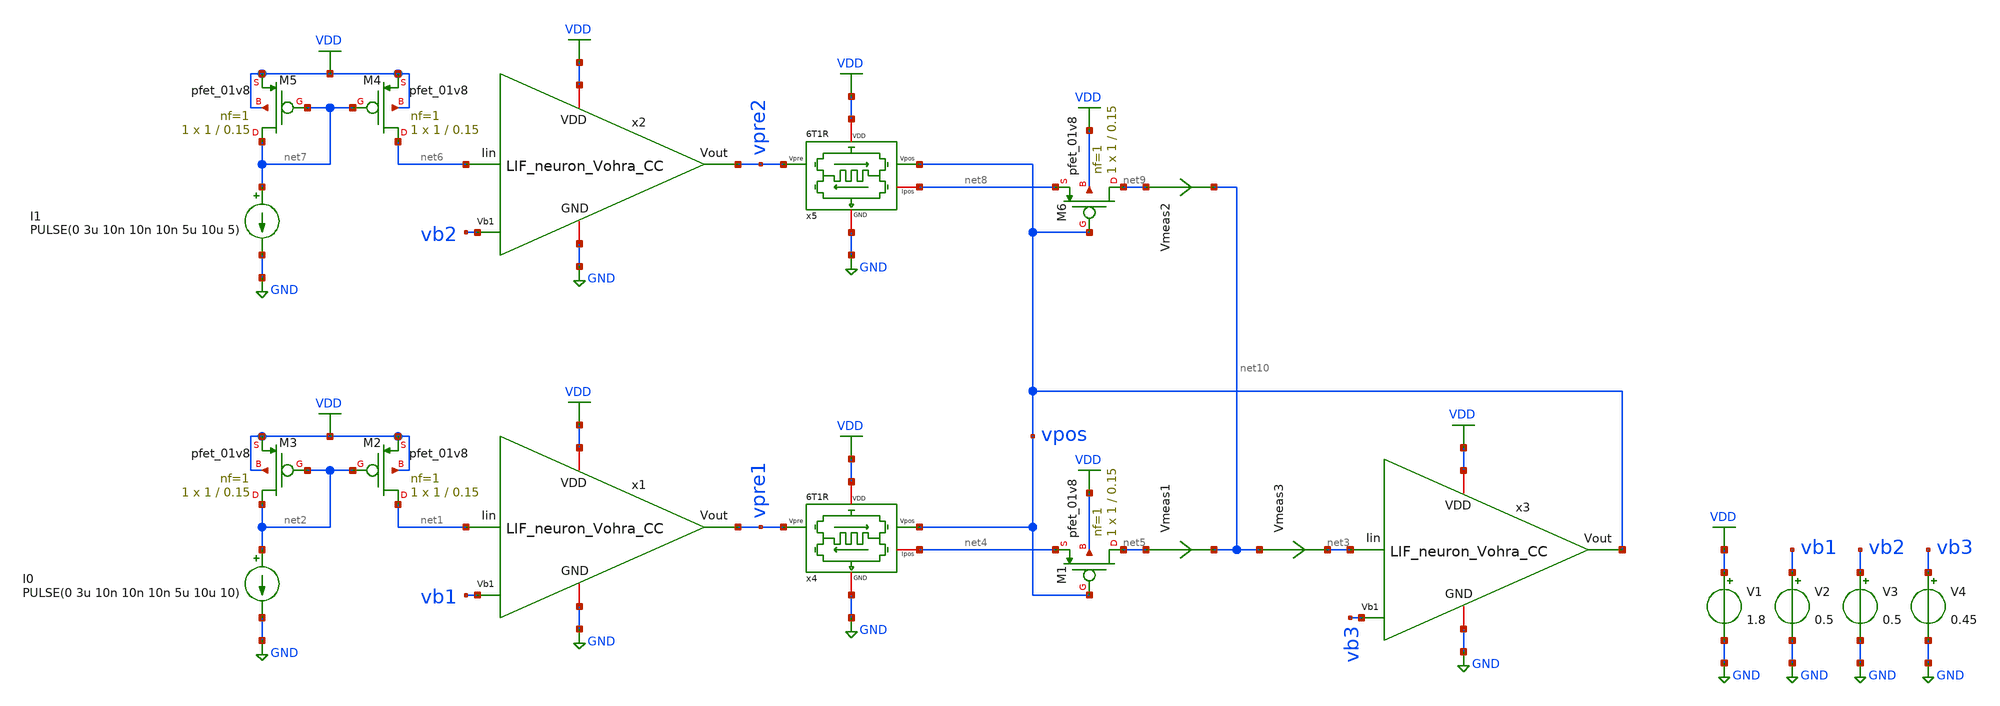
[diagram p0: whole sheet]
** sch_path: STDP/STDP_3_LIF_6T1R.sch
**.subckt STDP_3_LIF_6T1R
V1 VDD GND 1.8
V2 vb1 GND 0.5
x4 VDD net4 vpre1 vpos GND 6T1R
x1 VDD vpre1 vb1 GND net1 LIF_neuron_Vohra_CC
I0 net2 GND PULSE(0 3u 10n 10n 10n 5u 10u 10)
XM2 net1 net2 VDD VDD sky130_fd_pr__pfet_01v8 L=0.15 W=1 nf=1 ad='int((nf+1)/2) * W/nf * 0.29' as='int((nf+2)/2) * W/nf * 0.29'
+ pd='2*int((nf+1)/2) * (W/nf + 0.29)' ps='2*int((nf+2)/2) * (W/nf + 0.29)' nrd='0.29 / W' nrs='0.29 / W'
+ sa=0 sb=0 sd=0 mult=1 m=1
XM3 net2 net2 VDD VDD sky130_fd_pr__pfet_01v8 L=0.15 W=1 nf=1 ad='int((nf+1)/2) * W/nf * 0.29' as='int((nf+2)/2) * W/nf * 0.29'
+ pd='2*int((nf+1)/2) * (W/nf + 0.29)' ps='2*int((nf+2)/2) * (W/nf + 0.29)' nrd='0.29 / W' nrs='0.29 / W'
+ sa=0 sb=0 sd=0 mult=1 m=1
x3 VDD vpos vb3 GND net3 LIF_neuron_Vohra_CC
XM1 net5 vpos net4 VDD sky130_fd_pr__pfet_01v8 L=0.15 W=1 nf=1 ad='int((nf+1)/2) * W/nf * 0.29' as='int((nf+2)/2) * W/nf * 0.29'
+ pd='2*int((nf+1)/2) * (W/nf + 0.29)' ps='2*int((nf+2)/2) * (W/nf + 0.29)' nrd='0.29 / W' nrs='0.29 / W'
+ sa=0 sb=0 sd=0 mult=1 m=1
Vmeas1 net5 net10 0
.save i(vmeas1)
V3 vb2 GND 0.5
x5 VDD net8 vpre2 vpos GND 6T1R
x2 VDD vpre2 vb2 GND net6 LIF_neuron_Vohra_CC
I1 net7 GND PULSE(0 3u 10n 10n 10n 5u 10u 5)
XM4 net6 net7 VDD VDD sky130_fd_pr__pfet_01v8 L=0.15 W=1 nf=1 ad='int((nf+1)/2) * W/nf * 0.29' as='int((nf+2)/2) * W/nf * 0.29'
+ pd='2*int((nf+1)/2) * (W/nf + 0.29)' ps='2*int((nf+2)/2) * (W/nf + 0.29)' nrd='0.29 / W' nrs='0.29 / W'
+ sa=0 sb=0 sd=0 mult=1 m=1
XM5 net7 net7 VDD VDD sky130_fd_pr__pfet_01v8 L=0.15 W=1 nf=1 ad='int((nf+1)/2) * W/nf * 0.29' as='int((nf+2)/2) * W/nf * 0.29'
+ pd='2*int((nf+1)/2) * (W/nf + 0.29)' ps='2*int((nf+2)/2) * (W/nf + 0.29)' nrd='0.29 / W' nrs='0.29 / W'
+ sa=0 sb=0 sd=0 mult=1 m=1
XM6 net9 vpos net8 VDD sky130_fd_pr__pfet_01v8 L=0.15 W=1 nf=1 ad='int((nf+1)/2) * W/nf * 0.29' as='int((nf+2)/2) * W/nf * 0.29'
+ pd='2*int((nf+1)/2) * (W/nf + 0.29)' ps='2*int((nf+2)/2) * (W/nf + 0.29)' nrd='0.29 / W' nrs='0.29 / W'
+ sa=0 sb=0 sd=0 mult=1 m=1
Vmeas2 net9 net10 0
.save i(vmeas2)
V4 vb3 GND 0.45
Vmeas3 net10 net3 0
.save i(vmeas3)
**** begin user architecture code
.lib $::SKYWATER_MODELS/sky130.lib.spice tt

** opencircuitdesign pdks install
.inc $::SKYWATER_MODELS/rram_v0.spice



.control
  save all
  tran 20n 100u
  write STDP_3_LIF_6T1R.raw
.endc


**** end user architecture code
**.ends

* expanding   symbol:  /home/ricardo/RATT_repos/Proyectos_xschem/synapse/6T1R.sym # of pins=5
** sym_path: synapse/6T1R.sym
** sch_path: synapse/6T1R.sch
.subckt 6T1R VDD Ipos Vpre Vpos GND
*.ipin Vpre
*.ipin Vpos
*.iopin GND
*.iopin Ipos
*.iopin VDD
XM1 vipre Vpre net1 GND sky130_fd_pr__nfet_01v8 L=0.15 W=10 nf=1 ad='int((nf+1)/2) * W/nf * 0.29' as='int((nf+2)/2) * W/nf * 0.29'
+ pd='2*int((nf+1)/2) * (W/nf + 0.29)' ps='2*int((nf+2)/2) * (W/nf + 0.29)' nrd='0.29 / W' nrs='0.29 / W'
+ sa=0 sb=0 sd=0 mult=1 m=1
XR1 net2 net1 rram_v0
XM3 vipre Vpos net2 GND sky130_fd_pr__nfet_01v8 L=0.15 W=1 nf=1 ad='int((nf+1)/2) * W/nf * 0.29' as='int((nf+2)/2) * W/nf * 0.29'
+ pd='2*int((nf+1)/2) * (W/nf + 0.29)' ps='2*int((nf+2)/2) * (W/nf + 0.29)' nrd='0.29 / W' nrs='0.29 / W'
+ sa=0 sb=0 sd=0 mult=1 m=1
XM6 Ipos vipre VDD VDD sky130_fd_pr__pfet_01v8 L=0.15 W=1 nf=1 ad='int((nf+1)/2) * W/nf * 0.29' as='int((nf+2)/2) * W/nf * 0.29'
+ pd='2*int((nf+1)/2) * (W/nf + 0.29)' ps='2*int((nf+2)/2) * (W/nf + 0.29)' nrd='0.29 / W' nrs='0.29 / W'
+ sa=0 sb=0 sd=0 mult=1 m=1
XM5 vipre vipre VDD VDD sky130_fd_pr__pfet_01v8 L=0.15 W=20 nf=1 ad='int((nf+1)/2) * W/nf * 0.29' as='int((nf+2)/2) * W/nf * 0.29'
+ pd='2*int((nf+1)/2) * (W/nf + 0.29)' ps='2*int((nf+2)/2) * (W/nf + 0.29)' nrd='0.29 / W' nrs='0.29 / W'
+ sa=0 sb=0 sd=0 mult=1 m=1
XM2 net1 Vpos GND GND sky130_fd_pr__nfet_01v8 L=0.15 W=1 nf=1 ad='int((nf+1)/2) * W/nf * 0.29' as='int((nf+2)/2) * W/nf * 0.29'
+ pd='2*int((nf+1)/2) * (W/nf + 0.29)' ps='2*int((nf+2)/2) * (W/nf + 0.29)' nrd='0.29 / W' nrs='0.29 / W'
+ sa=0 sb=0 sd=0 mult=1 m=1
XM4 net2 Vpre GND GND sky130_fd_pr__nfet_01v8 L=0.15 W=10 nf=1 ad='int((nf+1)/2) * W/nf * 0.29' as='int((nf+2)/2) * W/nf * 0.29'
+ pd='2*int((nf+1)/2) * (W/nf + 0.29)' ps='2*int((nf+2)/2) * (W/nf + 0.29)' nrd='0.29 / W' nrs='0.29 / W'
+ sa=0 sb=0 sd=0 mult=1 m=1
.ends


* expanding   symbol:  /home/ricardo/RATT_repos/Proyectos_xschem/LIF_neuron/LIF_neuron_Vohra_CC.sym
*+ # of pins=5
** sym_path: LIF_neuron/LIF_neuron_Vohra_CC.sym
** sch_path: LIF_neuron/LIF_neuron_Vohra_CC.sch
.subckt LIF_neuron_Vohra_CC VDD Vout Vb1 GND Iin
*.iopin GND
*.ipin Vb1
*.iopin VDD
*.opin Vout
*.ipin Iin
XM8 net2 Vb1 GND GND sky130_fd_pr__nfet_01v8 L=0.5 W=5 nf=1 ad='int((nf+1)/2) * W/nf * 0.29' as='int((nf+2)/2) * W/nf * 0.29'
+ pd='2*int((nf+1)/2) * (W/nf + 0.29)' ps='2*int((nf+2)/2) * (W/nf + 0.29)' nrd='0.29 / W' nrs='0.29 / W'
+ sa=0 sb=0 sd=0 mult=1 m=1
XM7 rc net1 net2 GND sky130_fd_pr__nfet_01v8 L=1 W=1 nf=1 ad='int((nf+1)/2) * W/nf * 0.29' as='int((nf+2)/2) * W/nf * 0.29'
+ pd='2*int((nf+1)/2) * (W/nf + 0.29)' ps='2*int((nf+2)/2) * (W/nf + 0.29)' nrd='0.29 / W' nrs='0.29 / W'
+ sa=0 sb=0 sd=0 mult=1 m=1
XM6 rc net1 VDD VDD sky130_fd_pr__pfet_01v8 L=1 W=5 nf=1 ad='int((nf+1)/2) * W/nf * 0.29' as='int((nf+2)/2) * W/nf * 0.29'
+ pd='2*int((nf+1)/2) * (W/nf + 0.29)' ps='2*int((nf+2)/2) * (W/nf + 0.29)' nrd='0.29 / W' nrs='0.29 / W'
+ sa=0 sb=0 sd=0 mult=1 m=1
XCr rc GND sky130_fd_pr__cap_mim_m3_1 W=10 L=1 MF=1 m=1
XM9 Iin rc GND GND sky130_fd_pr__nfet_01v8 L=1 W=5 nf=1 ad='int((nf+1)/2) * W/nf * 0.29' as='int((nf+2)/2) * W/nf * 0.29'
+ pd='2*int((nf+1)/2) * (W/nf + 0.29)' ps='2*int((nf+2)/2) * (W/nf + 0.29)' nrd='0.29 / W' nrs='0.29 / W'
+ sa=0 sb=0 sd=0 mult=1 m=1
XCm Iin GND sky130_fd_pr__cap_mim_m3_1 W=30 L=1 MF=50 m=50
XM5 net3 Vout GND GND sky130_fd_pr__nfet_01v8 L=0.5 W=1 nf=1 ad='int((nf+1)/2) * W/nf * 0.29' as='int((nf+2)/2) * W/nf * 0.29'
+ pd='2*int((nf+1)/2) * (W/nf + 0.29)' ps='2*int((nf+2)/2) * (W/nf + 0.29)' nrd='0.29 / W' nrs='0.29 / W'
+ sa=0 sb=0 sd=0 mult=1 m=1
XM3 net1 Iin net3 GND sky130_fd_pr__nfet_01v8 L=1 W=1 nf=1 ad='int((nf+1)/2) * W/nf * 0.29' as='int((nf+2)/2) * W/nf * 0.29'
+ pd='2*int((nf+1)/2) * (W/nf + 0.29)' ps='2*int((nf+2)/2) * (W/nf + 0.29)' nrd='0.29 / W' nrs='0.29 / W'
+ sa=0 sb=0 sd=0 mult=1 m=1
XM1 net1 Iin VDD VDD sky130_fd_pr__pfet_01v8 L=1 W=1 nf=1 ad='int((nf+1)/2) * W/nf * 0.29' as='int((nf+2)/2) * W/nf * 0.29'
+ pd='2*int((nf+1)/2) * (W/nf + 0.29)' ps='2*int((nf+2)/2) * (W/nf + 0.29)' nrd='0.29 / W' nrs='0.29 / W'
+ sa=0 sb=0 sd=0 mult=1 m=1
XM4 Vout net1 net3 GND sky130_fd_pr__nfet_01v8 L=1 W=1 nf=1 ad='int((nf+1)/2) * W/nf * 0.29' as='int((nf+2)/2) * W/nf * 0.29'
+ pd='2*int((nf+1)/2) * (W/nf + 0.29)' ps='2*int((nf+2)/2) * (W/nf + 0.29)' nrd='0.29 / W' nrs='0.29 / W'
+ sa=0 sb=0 sd=0 mult=1 m=1
XM2 Vout net1 VDD VDD sky130_fd_pr__pfet_01v8 L=1 W=5 nf=1 ad='int((nf+1)/2) * W/nf * 0.29' as='int((nf+2)/2) * W/nf * 0.29'
+ pd='2*int((nf+1)/2) * (W/nf + 0.29)' ps='2*int((nf+2)/2) * (W/nf + 0.29)' nrd='0.29 / W' nrs='0.29 / W'
+ sa=0 sb=0 sd=0 mult=1 m=1
.ends

.GLOBAL GND
.GLOBAL VDD
.end
